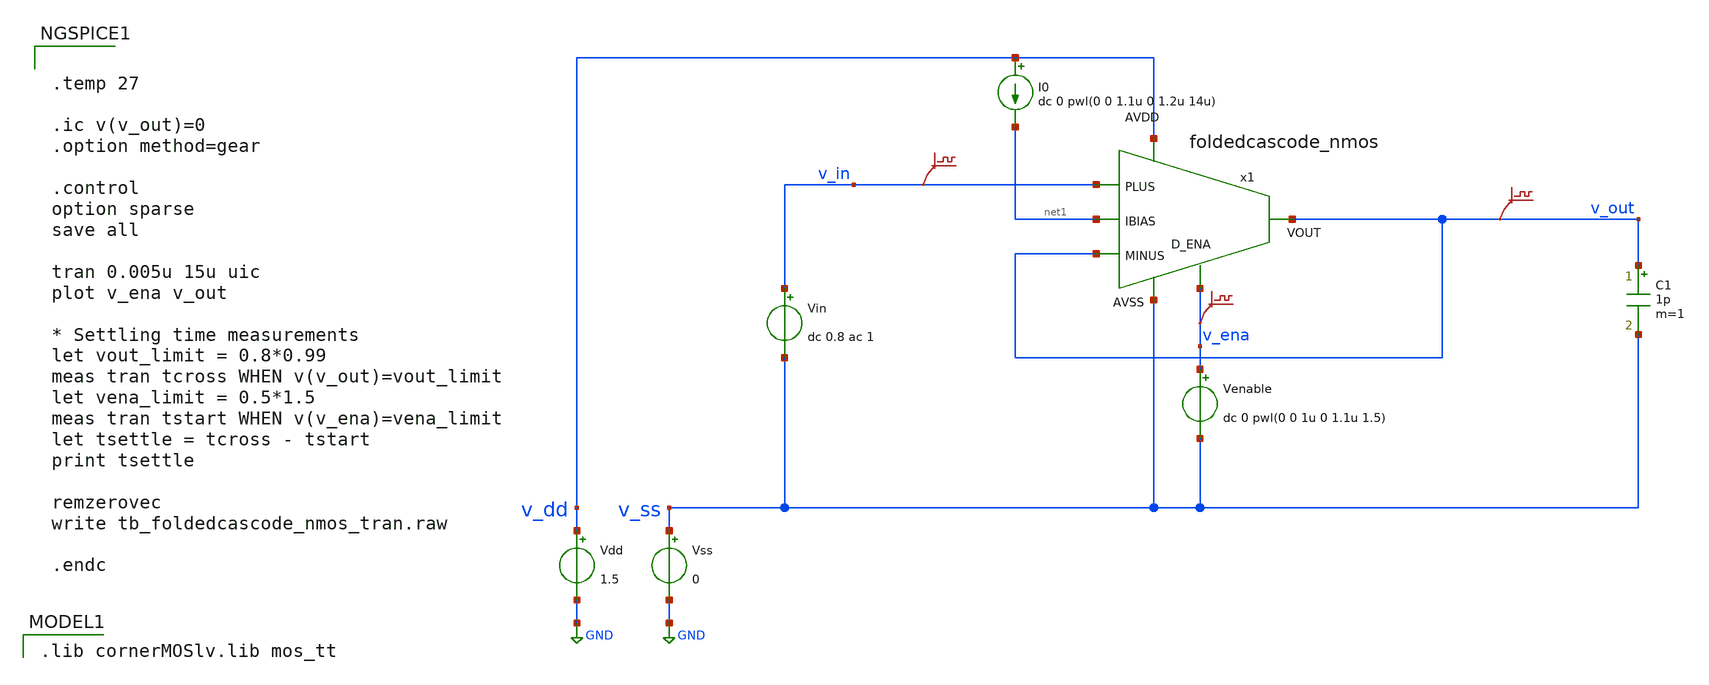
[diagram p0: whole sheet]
** sch_path: Designs/otas/1_schematics/tb_foldedcascode_nmos_tran.sch
* (c) 2025 Thesis_HP, Apache-2.0 license
**.subckt tb_foldedcascode_nmos_tran
Vdd v_dd GND 1.5
Vss v_ss GND 0
C1 v_out v_ss 1p m=1
Vin v_in v_ss dc 0.8 ac 1
.save v(v_in)
.save v(v_out)
Venable v_ena v_ss dc 0 pwl(0 0 1u 0 1.1u 1.5)
.save v(v_ena)
I0 v_dd net1 dc 0 pwl(0 0 1.1u 0 1.2u 14u)
x1 v_dd net1 v_out v_out v_in v_ena v_ss foldedcascode_nmos
**** begin user architecture code
 .lib cornerMOSlv.lib mos_tt



.temp 27

.ic v(v_out)=0
.option method=gear

.control
option sparse
save all

tran 0.005u 15u uic
plot v_ena v_out

* Settling time measurements
let vout_limit = 0.8*0.99
meas tran tcross WHEN v(v_out)=vout_limit
let vena_limit = 0.5*1.5
meas tran tstart WHEN v(v_ena)=vena_limit
let tsettle = tcross - tstart
print tsettle

remzerovec
write tb_foldedcascode_nmos_tran.raw

.endc


**** end user architecture code
**.ends
.GLOBAL GND
.end
